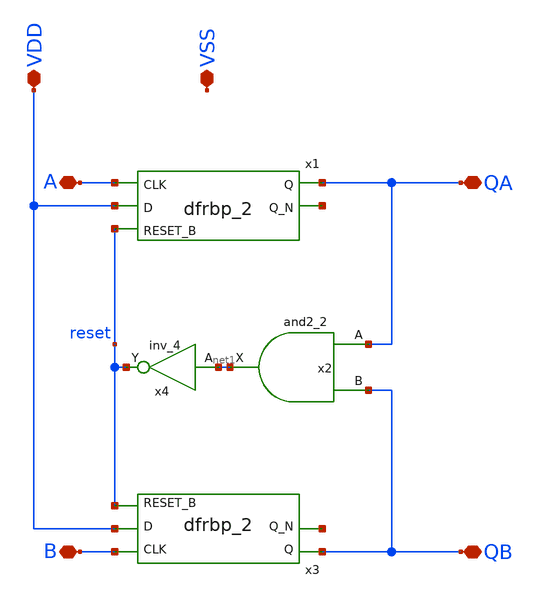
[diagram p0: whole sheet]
** sch_path: xschem/pfd/pfd.sch
**.subckt pfd VDD A B QA QB VSS
*.iopin VDD
*.iopin A
*.iopin B
*.iopin QA
*.iopin QB
*.iopin VSS
x1 A VDD reset VSS VSS VDD VDD QA net2 sky130_fd_sc_hd__dfrbp_2
x2 QA QB VSS VSS VDD VDD net1 sky130_fd_sc_hd__and2_2
x3 B VDD reset VSS VSS VDD VDD QB net3 sky130_fd_sc_hd__dfrbp_2
x4 net1 VSS VSS VDD VDD reset sky130_fd_sc_hd__inv_4
**.ends
.end
